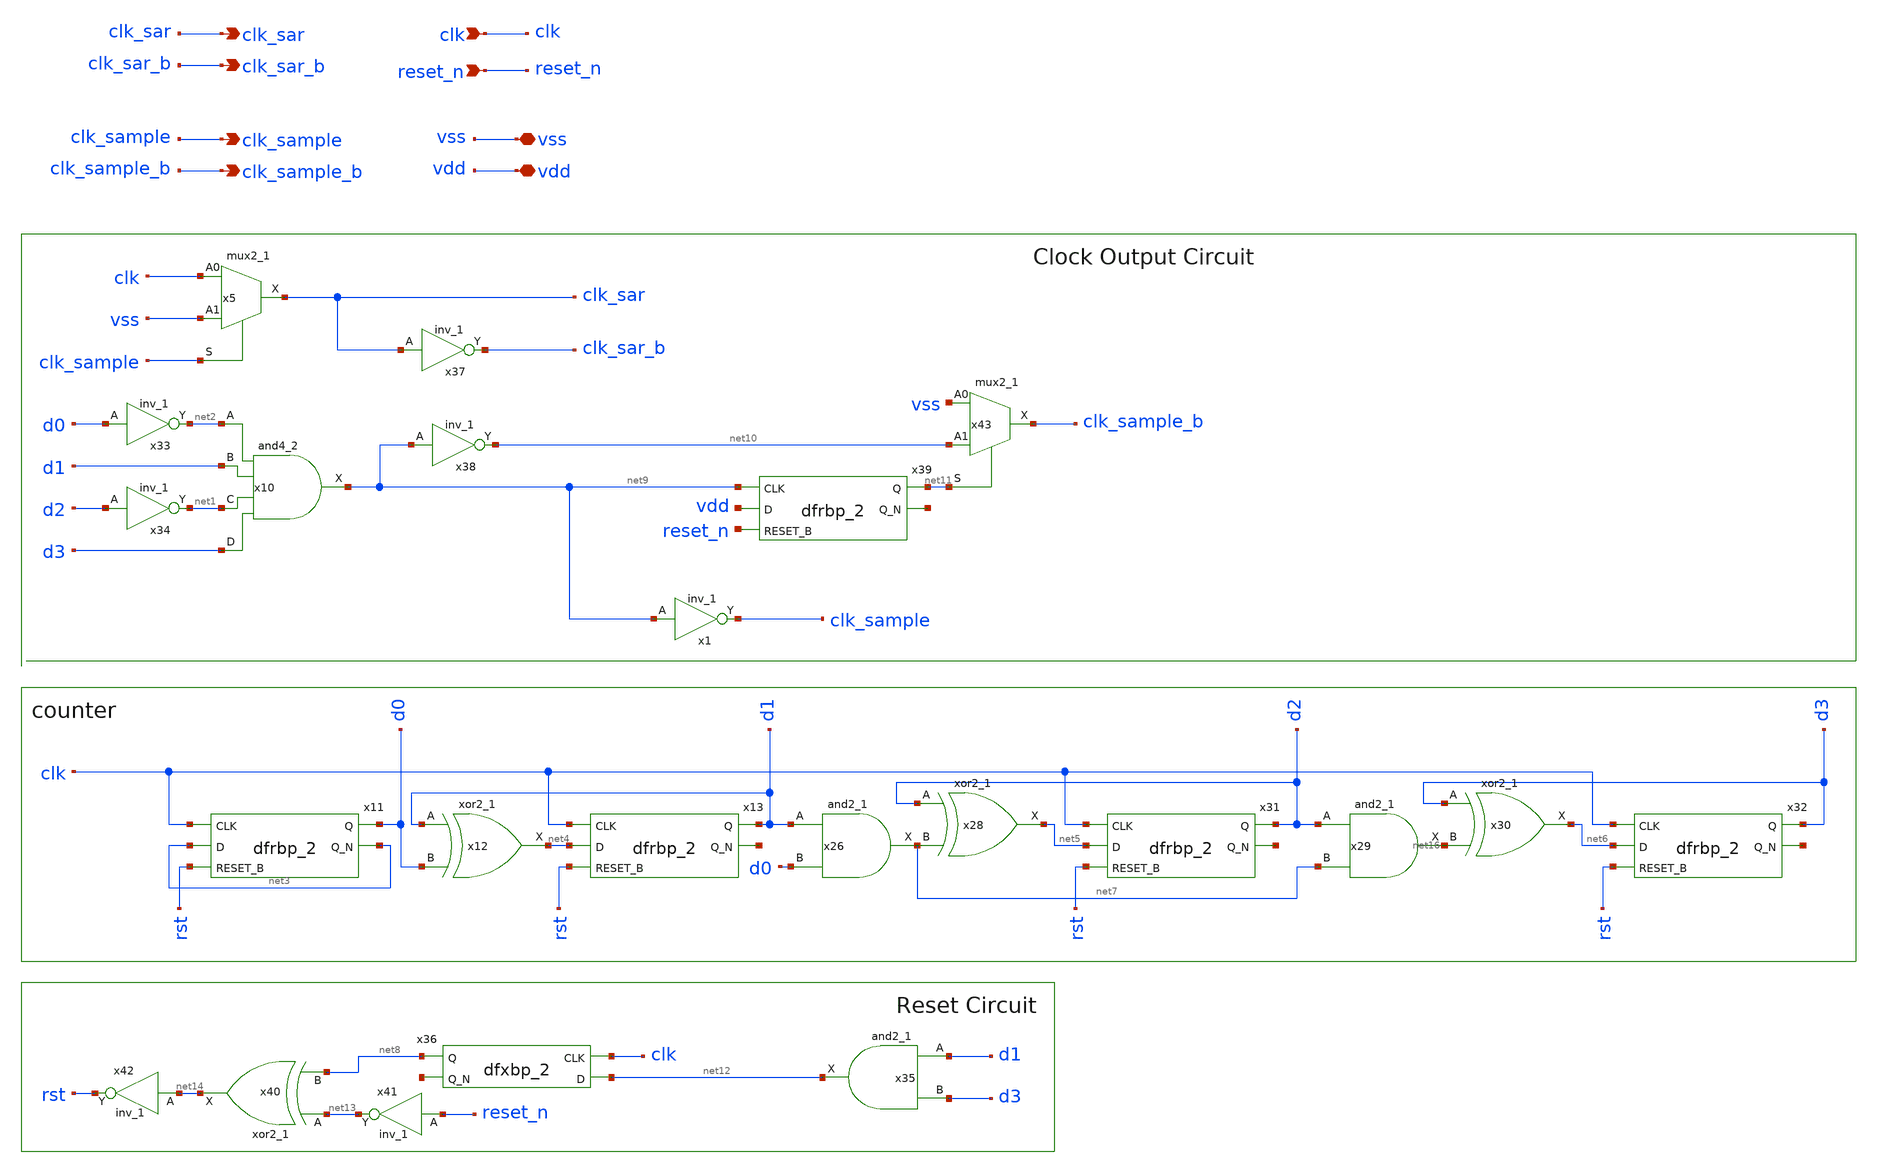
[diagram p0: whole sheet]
** sch_path: xschem/clockgen/clockgen.sch
**.subckt clockgen clk_sar clk_sample clk vss vdd clk_sar_b clk_sample_b reset_n
*.opin clk_sar
*.opin clk_sample
*.ipin clk
*.iopin vss
*.iopin vdd
*.opin clk_sar_b
*.opin clk_sample_b
*.ipin reset_n
x5 clk vss clk_sample vss vss vdd vdd clk_sar sky130_fd_sc_hd__mux2_1
x10 net2 d1 net1 d3 vss vss vdd vdd net9 sky130_fd_sc_hd__and4_2
x11 clk net3 rst vss vss vdd vdd d0 net3 sky130_fd_sc_hd__dfrbp_2
x12 d1 d0 vss vss vdd vdd net4 sky130_fd_sc_hd__xor2_1
x13 clk net4 rst vss vss vdd vdd d1 net15 sky130_fd_sc_hd__dfrbp_2
x26 d1 d0 vss vss vdd vdd net7 sky130_fd_sc_hd__and2_1
x28 d2 net7 vss vss vdd vdd net5 sky130_fd_sc_hd__xor2_1
x29 d2 net7 vss vss vdd vdd net16 sky130_fd_sc_hd__and2_1
x30 d3 net16 vss vss vdd vdd net6 sky130_fd_sc_hd__xor2_1
x31 clk net5 rst vss vss vdd vdd d2 net17 sky130_fd_sc_hd__dfrbp_2
x32 clk net6 rst vss vss vdd vdd d3 net18 sky130_fd_sc_hd__dfrbp_2
x33 d0 vss vss vdd vdd net2 sky130_fd_sc_hd__inv_1
x34 d2 vss vss vdd vdd net1 sky130_fd_sc_hd__inv_1
x35 d1 d3 vss vss vdd vdd net12 sky130_fd_sc_hd__and2_1
x36 clk net12 vss vss vdd vdd net8 net19 sky130_fd_sc_hd__dfxbp_2
x37 clk_sar vss vss vdd vdd clk_sar_b sky130_fd_sc_hd__inv_1
x38 net9 vss vss vdd vdd net10 sky130_fd_sc_hd__inv_1
x39 net9 vdd reset_n vss vss vdd vdd net11 net20 sky130_fd_sc_hd__dfrbp_2
x40 net13 net8 vss vss vdd vdd net14 sky130_fd_sc_hd__xor2_1
x41 reset_n vss vss vdd vdd net13 sky130_fd_sc_hd__inv_1
x42 net14 vss vss vdd vdd rst sky130_fd_sc_hd__inv_1
x43 vss net10 net11 vss vss vdd vdd clk_sample_b sky130_fd_sc_hd__mux2_1
x1 net9 vss vss vdd vdd clk_sample sky130_fd_sc_hd__inv_1
**.ends
.end
